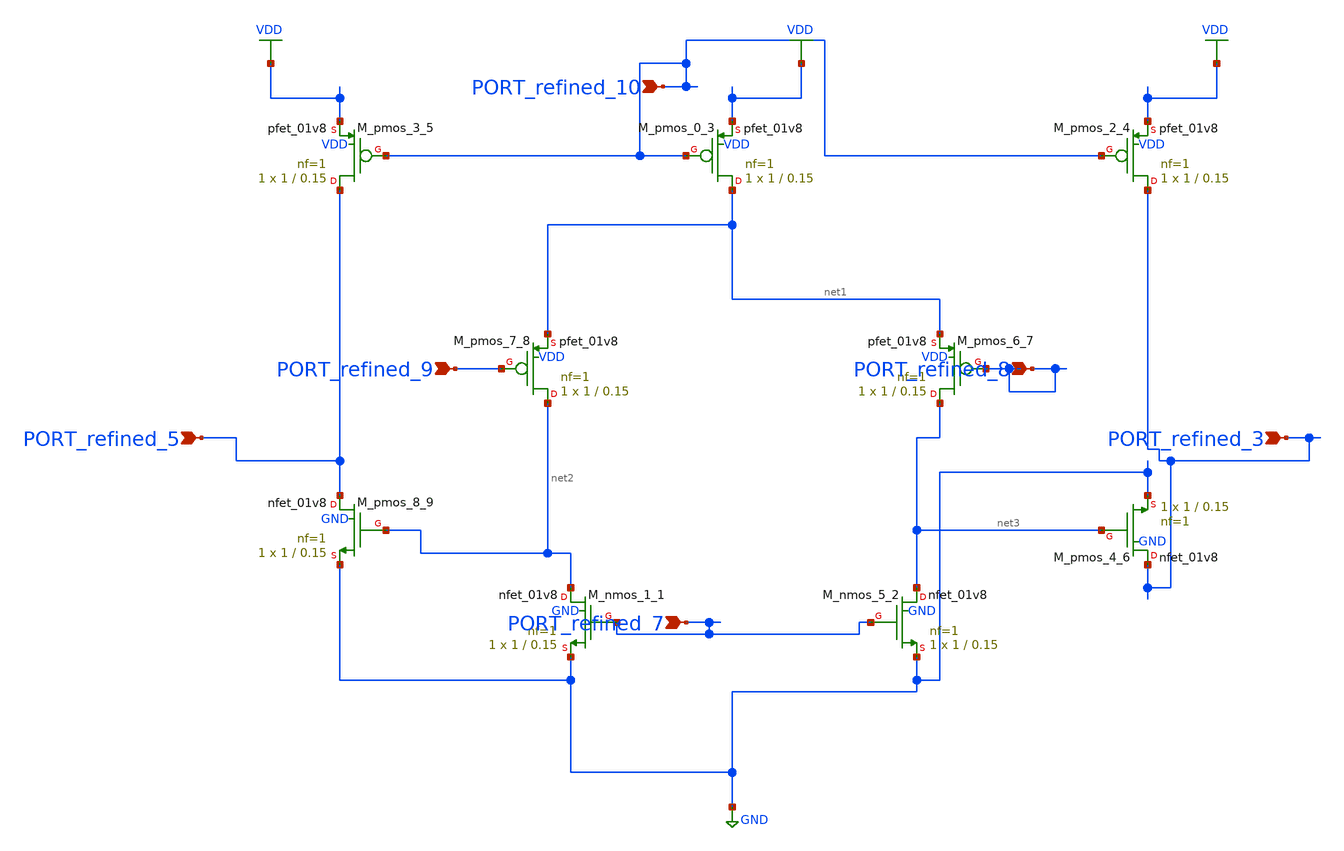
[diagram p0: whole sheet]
** sch_path: schematics/SchemGen/p04_fig5_opamp.sch
**.subckt p04_fig5_opamp PORT_refined_8 PORT_refined_3 PORT_refined_9 PORT_refined_5 PORT_refined_7
*+ PORT_refined_10
*.ipin PORT_refined_8
*.ipin PORT_refined_3
*.ipin PORT_refined_9
*.ipin PORT_refined_5
*.ipin PORT_refined_7
*.ipin PORT_refined_10
XM_nmos_1_1 net2 PORT_refined_7 GND GND sky130_fd_pr__nfet_01v8 L=0.15 W=1 nf=1 ad='int((1 + 1)/2) * 1 / 1 * 0.29'
+ as='int((1 + 2)/2) * 1 / 1 * 0.29' pd='2*int((1 + 1)/2) * (1 / 1 + 0.29)' ps='2*int((1 + 2)/2) * (1 / 1 + 0.29)'
+ nrd='0.29 / 1 ' nrs='0.29 / 1 ' sa=0 sb=0 sd=0 mult=1 m=1
XM_nmos_5_2 net3 PORT_refined_7 GND GND sky130_fd_pr__nfet_01v8 L=0.15 W=1 nf=1 ad='int((1 + 1)/2) * 1 / 1 * 0.29'
+ as='int((1 + 2)/2) * 1 / 1 * 0.29' pd='2*int((1 + 1)/2) * (1 / 1 + 0.29)' ps='2*int((1 + 2)/2) * (1 / 1 + 0.29)'
+ nrd='0.29 / 1 ' nrs='0.29 / 1 ' sa=0 sb=0 sd=0 mult=1 m=1
XM_pmos_0_3 net1 PORT_refined_10 VDD VDD sky130_fd_pr__pfet_01v8 L=0.15 W=1 nf=1 ad='int((1 + 1)/2) * 1 / 1 * 0.29'
+ as='int((1 + 2)/2) * 1 / 1 * 0.29' pd='2*int((1 + 1)/2) * (1 / 1 + 0.29)' ps='2*int((1 + 2)/2) * (1 / 1 + 0.29)'
+ nrd='0.29 / 1 ' nrs='0.29 / 1 ' sa=0 sb=0 sd=0 mult=1 m=1
XM_pmos_2_4 PORT_refined_3 PORT_refined_10 VDD VDD sky130_fd_pr__pfet_01v8 L=0.15 W=1 nf=1 ad='int((1 + 1)/2) * 1 / 1 * 0.29'
+ as='int((1 + 2)/2) * 1 / 1 * 0.29' pd='2*int((1 + 1)/2) * (1 / 1 + 0.29)' ps='2*int((1 + 2)/2) * (1 / 1 + 0.29)'
+ nrd='0.29 / 1 ' nrs='0.29 / 1 ' sa=0 sb=0 sd=0 mult=1 m=1
XM_pmos_3_5 PORT_refined_5 PORT_refined_10 VDD VDD sky130_fd_pr__pfet_01v8 L=0.15 W=1 nf=1 ad='int((1 + 1)/2) * 1 / 1 * 0.29'
+ as='int((1 + 2)/2) * 1 / 1 * 0.29' pd='2*int((1 + 1)/2) * (1 / 1 + 0.29)' ps='2*int((1 + 2)/2) * (1 / 1 + 0.29)'
+ nrd='0.29 / 1 ' nrs='0.29 / 1 ' sa=0 sb=0 sd=0 mult=1 m=1
XM_pmos_4_6 PORT_refined_3 net3 GND GND sky130_fd_pr__nfet_01v8 L=0.15 W=1 nf=1 ad='int((1 + 1)/2) * 1 / 1 * 0.29'
+ as='int((1 + 2)/2) * 1 / 1 * 0.29' pd='2*int((1 + 1)/2) * (1 / 1 + 0.29)' ps='2*int((1 + 2)/2) * (1 / 1 + 0.29)'
+ nrd='0.29 / 1 ' nrs='0.29 / 1 ' sa=0 sb=0 sd=0 mult=1 m=1
XM_pmos_6_7 net3 PORT_refined_8 net1 VDD sky130_fd_pr__pfet_01v8 L=0.15 W=1 nf=1 ad='int((1 + 1)/2) * 1 / 1 * 0.29'
+ as='int((1 + 2)/2) * 1 / 1 * 0.29' pd='2*int((1 + 1)/2) * (1 / 1 + 0.29)' ps='2*int((1 + 2)/2) * (1 / 1 + 0.29)'
+ nrd='0.29 / 1 ' nrs='0.29 / 1 ' sa=0 sb=0 sd=0 mult=1 m=1
XM_pmos_7_8 net2 PORT_refined_9 net1 VDD sky130_fd_pr__pfet_01v8 L=0.15 W=1 nf=1 ad='int((1 + 1)/2) * 1 / 1 * 0.29'
+ as='int((1 + 2)/2) * 1 / 1 * 0.29' pd='2*int((1 + 1)/2) * (1 / 1 + 0.29)' ps='2*int((1 + 2)/2) * (1 / 1 + 0.29)'
+ nrd='0.29 / 1 ' nrs='0.29 / 1 ' sa=0 sb=0 sd=0 mult=1 m=1
XM_pmos_8_9 PORT_refined_5 net2 GND GND sky130_fd_pr__nfet_01v8 L=0.15 W=1 nf=1 ad='int((1 + 1)/2) * 1 / 1 * 0.29'
+ as='int((1 + 2)/2) * 1 / 1 * 0.29' pd='2*int((1 + 1)/2) * (1 / 1 + 0.29)' ps='2*int((1 + 2)/2) * (1 / 1 + 0.29)'
+ nrd='0.29 / 1 ' nrs='0.29 / 1 ' sa=0 sb=0 sd=0 mult=1 m=1
**.ends
.GLOBAL GND
.GLOBAL VDD
.end
